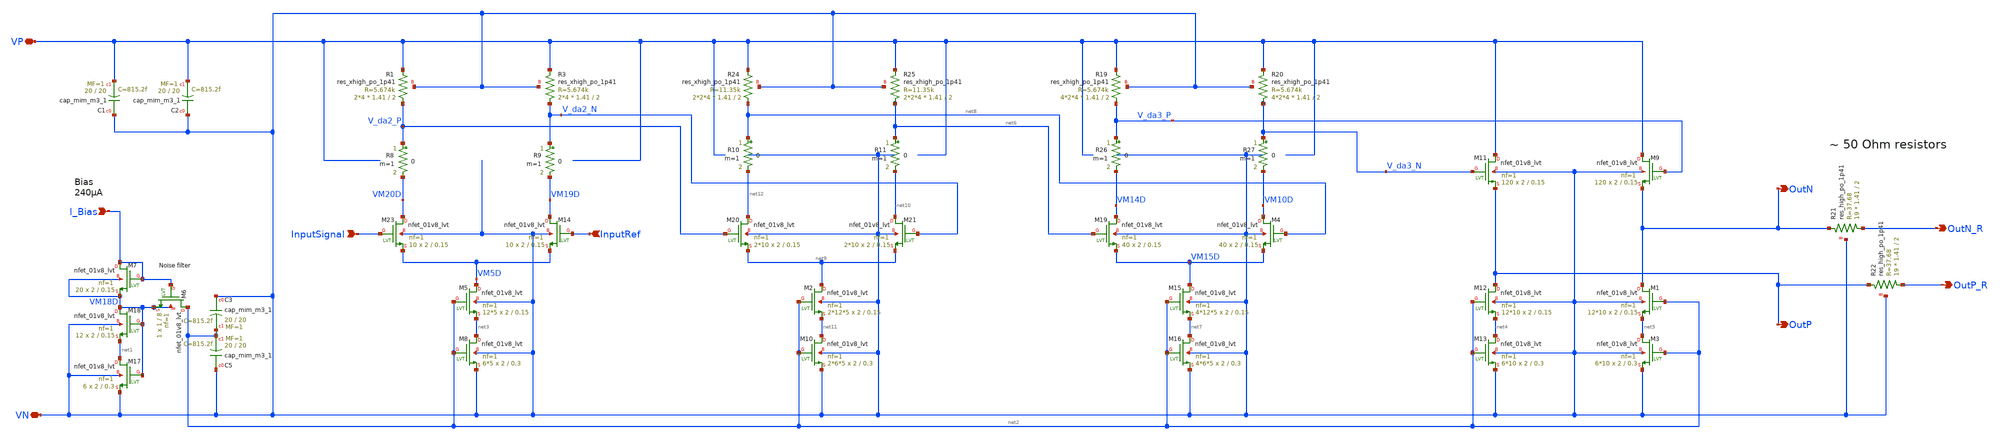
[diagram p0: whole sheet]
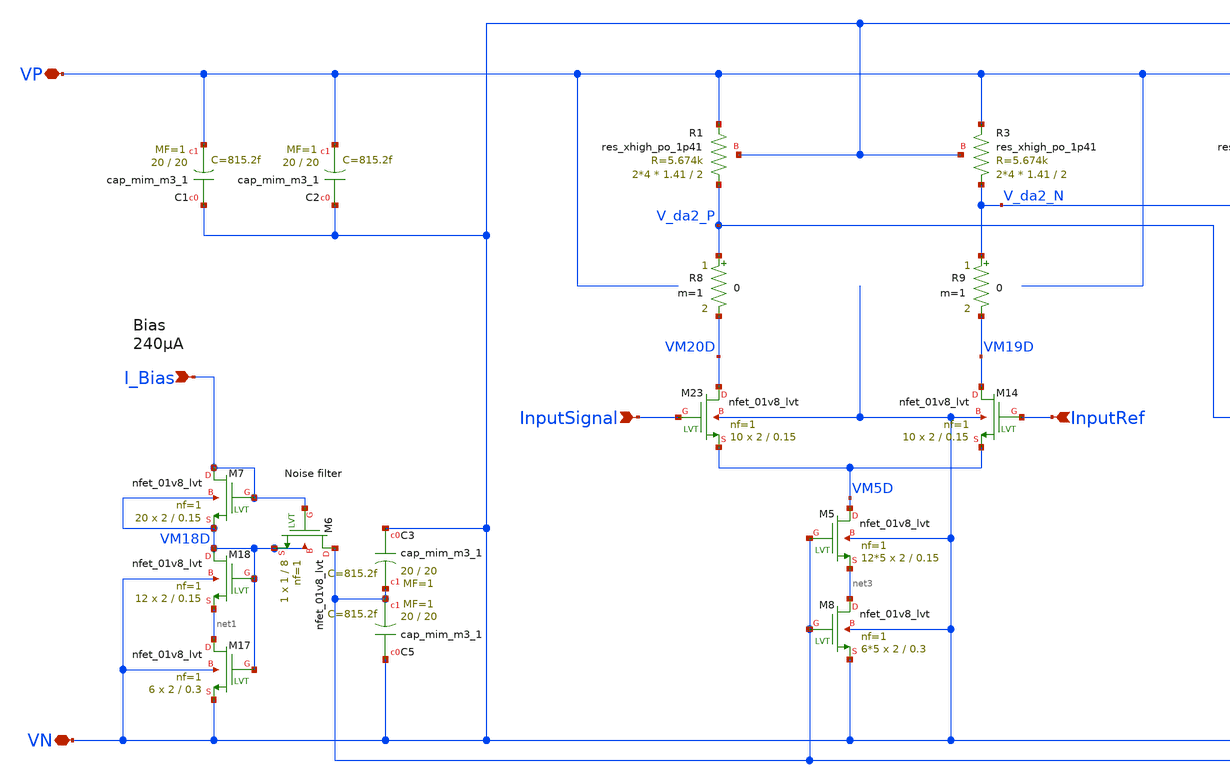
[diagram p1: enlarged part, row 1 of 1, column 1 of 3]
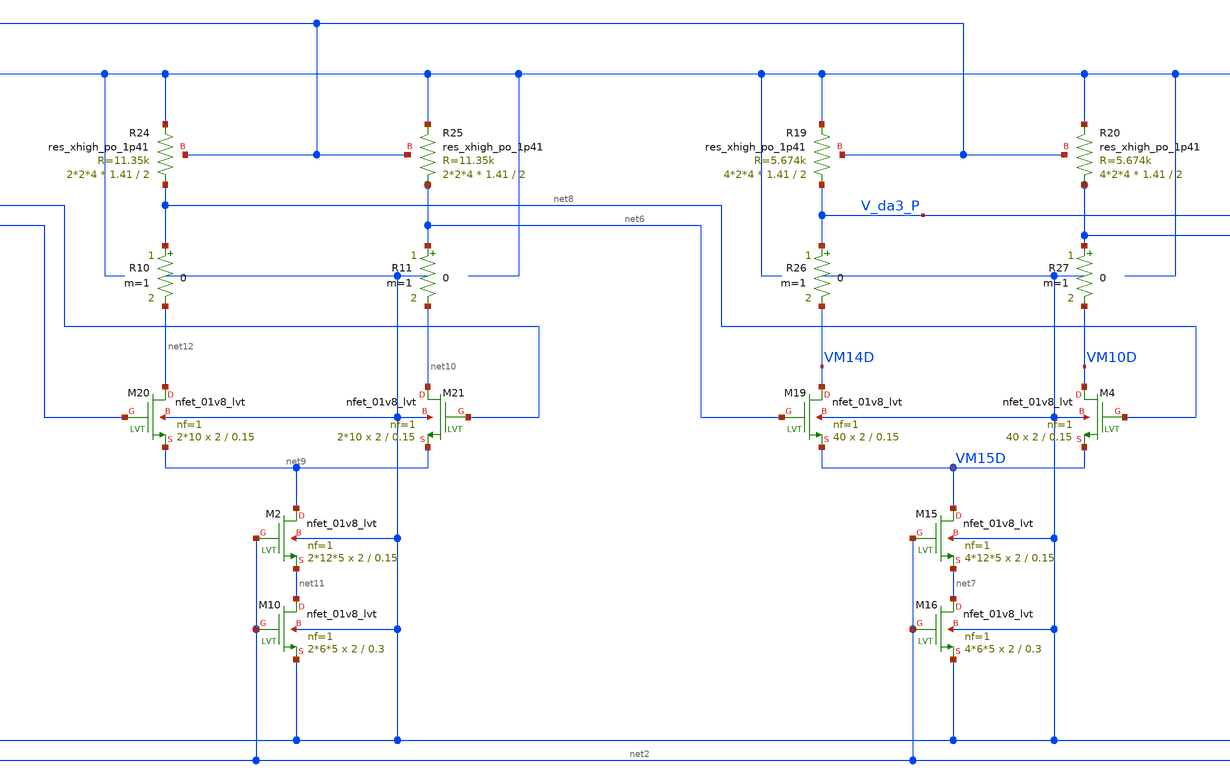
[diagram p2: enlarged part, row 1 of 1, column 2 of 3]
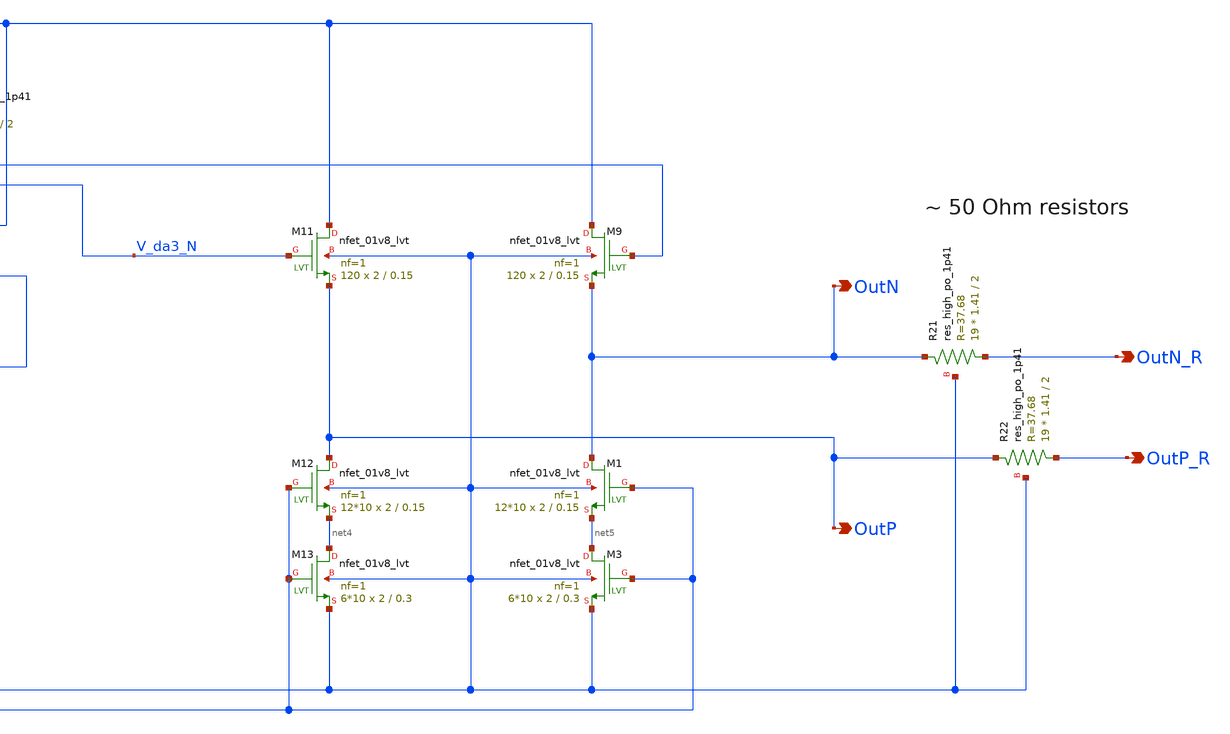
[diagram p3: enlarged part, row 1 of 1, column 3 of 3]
** sch_path: xschem/outdriver/outdriver_v4.sch
**.subckt outdriver_v4 VN InputRef VP I_Bias InputSignal OutN OutP OutN_R OutP_R
*.iopin VN
*.ipin InputRef
*.iopin VP
*.ipin I_Bias
*.ipin InputSignal
*.opin OutN
*.opin OutP
*.opin OutN_R
*.opin OutP_R
XC5 VN net2 sky130_fd_pr__cap_mim_m3_1 W=20 L=20 MF=1 m=1
XC3 VN net2 sky130_fd_pr__cap_mim_m3_1 W=20 L=20 MF=1 m=1
XM17 net1 VM18D VN VN sky130_fd_pr__nfet_01v8_lvt L=0.3 W=2 nf=1 ad='int((nf+1)/2) * W/nf * 0.29' as='int((nf+2)/2) * W/nf * 0.29'
+ pd='2*int((nf+1)/2) * (W/nf + 0.29)' ps='2*int((nf+2)/2) * (W/nf + 0.29)' nrd='0.29 / W' nrs='0.29 / W'
+ sa=0 sb=0 sd=0 mult=6 m=6
XM18 VM18D VM18D net1 VN sky130_fd_pr__nfet_01v8_lvt L=0.15 W=2 nf=1 ad='int((nf+1)/2) * W/nf * 0.29'
+ as='int((nf+2)/2) * W/nf * 0.29' pd='2*int((nf+1)/2) * (W/nf + 0.29)' ps='2*int((nf+2)/2) * (W/nf + 0.29)'
+ nrd='0.29 / W' nrs='0.29 / W' sa=0 sb=0 sd=0 mult=12 m=12
XM7 I_Bias I_Bias VM18D VM18D sky130_fd_pr__nfet_01v8_lvt L=0.15 W=2 nf=1 ad='int((nf+1)/2) * W/nf * 0.29'
+ as='int((nf+2)/2) * W/nf * 0.29' pd='2*int((nf+1)/2) * (W/nf + 0.29)' ps='2*int((nf+2)/2) * (W/nf + 0.29)'
+ nrd='0.29 / W' nrs='0.29 / W' sa=0 sb=0 sd=0 mult=20 m=20
XM5 VM5D net2 net3 VN sky130_fd_pr__nfet_01v8_lvt L=0.15 W=2 nf=1 ad='int((nf+1)/2) * W/nf * 0.29' as='int((nf+2)/2) * W/nf * 0.29'
+ pd='2*int((nf+1)/2) * (W/nf + 0.29)' ps='2*int((nf+2)/2) * (W/nf + 0.29)' nrd='0.29 / W' nrs='0.29 / W'
+ sa=0 sb=0 sd=0 mult=12*5 m=12*5
XM8 net3 net2 VN VN sky130_fd_pr__nfet_01v8_lvt L=0.3 W=2 nf=1 ad='int((nf+1)/2) * W/nf * 0.29' as='int((nf+2)/2) * W/nf * 0.29'
+ pd='2*int((nf+1)/2) * (W/nf + 0.29)' ps='2*int((nf+2)/2) * (W/nf + 0.29)' nrd='0.29 / W' nrs='0.29 / W'
+ sa=0 sb=0 sd=0 mult=6*5 m=6*5
XR1 V_da2_P VP VN sky130_fd_pr__res_xhigh_po_1p41 L=2 mult=2*4 m=2*4
XR3 V_da2_N VP VN sky130_fd_pr__res_xhigh_po_1p41 L=2 mult=2*4 m=2*4
XM9 VP V_da3_P OutN VN sky130_fd_pr__nfet_01v8_lvt L=0.15 W=2 nf=1 ad='int((nf+1)/2) * W/nf * 0.29' as='int((nf+2)/2) * W/nf * 0.29'
+ pd='2*int((nf+1)/2) * (W/nf + 0.29)' ps='2*int((nf+2)/2) * (W/nf + 0.29)' nrd='0.29 / W' nrs='0.29 / W'
+ sa=0 sb=0 sd=0 mult=120 m=120
XM11 VP V_da3_N OutP VN sky130_fd_pr__nfet_01v8_lvt L=0.15 W=2 nf=1 ad='int((nf+1)/2) * W/nf * 0.29'
+ as='int((nf+2)/2) * W/nf * 0.29' pd='2*int((nf+1)/2) * (W/nf + 0.29)' ps='2*int((nf+2)/2) * (W/nf + 0.29)'
+ nrd='0.29 / W' nrs='0.29 / W' sa=0 sb=0 sd=0 mult=120 m=120
XM12 OutP net2 net4 VN sky130_fd_pr__nfet_01v8_lvt L=0.15 W=2 nf=1 ad='int((nf+1)/2) * W/nf * 0.29' as='int((nf+2)/2) * W/nf * 0.29'
+ pd='2*int((nf+1)/2) * (W/nf + 0.29)' ps='2*int((nf+2)/2) * (W/nf + 0.29)' nrd='0.29 / W' nrs='0.29 / W'
+ sa=0 sb=0 sd=0 mult=12*10 m=12*10
XM13 net4 net2 VN VN sky130_fd_pr__nfet_01v8_lvt L=0.3 W=2 nf=1 ad='int((nf+1)/2) * W/nf * 0.29' as='int((nf+2)/2) * W/nf * 0.29'
+ pd='2*int((nf+1)/2) * (W/nf + 0.29)' ps='2*int((nf+2)/2) * (W/nf + 0.29)' nrd='0.29 / W' nrs='0.29 / W'
+ sa=0 sb=0 sd=0 mult=6*10 m=6*10
XM1 OutN net2 net5 VN sky130_fd_pr__nfet_01v8_lvt L=0.15 W=2 nf=1 ad='int((nf+1)/2) * W/nf * 0.29' as='int((nf+2)/2) * W/nf * 0.29'
+ pd='2*int((nf+1)/2) * (W/nf + 0.29)' ps='2*int((nf+2)/2) * (W/nf + 0.29)' nrd='0.29 / W' nrs='0.29 / W'
+ sa=0 sb=0 sd=0 mult=12*10 m=12*10
XM3 net5 net2 VN VN sky130_fd_pr__nfet_01v8_lvt L=0.3 W=2 nf=1 ad='int((nf+1)/2) * W/nf * 0.29' as='int((nf+2)/2) * W/nf * 0.29'
+ pd='2*int((nf+1)/2) * (W/nf + 0.29)' ps='2*int((nf+2)/2) * (W/nf + 0.29)' nrd='0.29 / W' nrs='0.29 / W'
+ sa=0 sb=0 sd=0 mult=6*10 m=6*10
XM6 net2 I_Bias VM18D VM18D sky130_fd_pr__nfet_01v8_lvt L=8 W=1 nf=1 ad='int((nf+1)/2) * W/nf * 0.29'
+ as='int((nf+2)/2) * W/nf * 0.29' pd='2*int((nf+1)/2) * (W/nf + 0.29)' ps='2*int((nf+2)/2) * (W/nf + 0.29)'
+ nrd='0.29 / W' nrs='0.29 / W' sa=0 sb=0 sd=0 mult=1 m=1
XC1 VN VP sky130_fd_pr__cap_mim_m3_1 W=20 L=20 MF=1 m=1
XC2 VN VP sky130_fd_pr__cap_mim_m3_1 W=20 L=20 MF=1 m=1
XM15 VM15D net2 net7 VN sky130_fd_pr__nfet_01v8_lvt L=0.15 W=2 nf=1 ad='int((nf+1)/2) * W/nf * 0.29'
+ as='int((nf+2)/2) * W/nf * 0.29' pd='2*int((nf+1)/2) * (W/nf + 0.29)' ps='2*int((nf+2)/2) * (W/nf + 0.29)'
+ nrd='0.29 / W' nrs='0.29 / W' sa=0 sb=0 sd=0 mult=4*12*5 m=4*12*5
XM16 net7 net2 VN VN sky130_fd_pr__nfet_01v8_lvt L=0.3 W=2 nf=1 ad='int((nf+1)/2) * W/nf * 0.29' as='int((nf+2)/2) * W/nf * 0.29'
+ pd='2*int((nf+1)/2) * (W/nf + 0.29)' ps='2*int((nf+2)/2) * (W/nf + 0.29)' nrd='0.29 / W' nrs='0.29 / W'
+ sa=0 sb=0 sd=0 mult=4*6*5 m=4*6*5
XR19 V_da3_P VP VN sky130_fd_pr__res_xhigh_po_1p41 L=2 mult=4*2*4 m=4*2*4
XR20 V_da3_N VP VN sky130_fd_pr__res_xhigh_po_1p41 L=2 mult=4*2*4 m=4*2*4
XM4 VM10D net8 VM15D VN sky130_fd_pr__nfet_01v8_lvt L=0.15 W=2 nf=1 ad='int((nf+1)/2) * W/nf * 0.29'
+ as='int((nf+2)/2) * W/nf * 0.29' pd='2*int((nf+1)/2) * (W/nf + 0.29)' ps='2*int((nf+2)/2) * (W/nf + 0.29)'
+ nrd='0.29 / W' nrs='0.29 / W' sa=0 sb=0 sd=0 mult=40 m=40
XR21 OutN_R OutN VN sky130_fd_pr__res_high_po_1p41 L=2 mult=19 m=19
XR22 OutP_R OutP VN sky130_fd_pr__res_high_po_1p41 L=2 mult=19 m=19
XM2 net9 net2 net11 VN sky130_fd_pr__nfet_01v8_lvt L=0.15 W=2 nf=1 ad='int((nf+1)/2) * W/nf * 0.29' as='int((nf+2)/2) * W/nf * 0.29'
+ pd='2*int((nf+1)/2) * (W/nf + 0.29)' ps='2*int((nf+2)/2) * (W/nf + 0.29)' nrd='0.29 / W' nrs='0.29 / W'
+ sa=0 sb=0 sd=0 mult=2*12*5 m=2*12*5
XM10 net11 net2 VN VN sky130_fd_pr__nfet_01v8_lvt L=0.3 W=2 nf=1 ad='int((nf+1)/2) * W/nf * 0.29' as='int((nf+2)/2) * W/nf * 0.29'
+ pd='2*int((nf+1)/2) * (W/nf + 0.29)' ps='2*int((nf+2)/2) * (W/nf + 0.29)' nrd='0.29 / W' nrs='0.29 / W'
+ sa=0 sb=0 sd=0 mult=2*6*5 m=2*6*5
XR24 net8 VP VN sky130_fd_pr__res_xhigh_po_1p41 L=2 mult=2*2*4 m=2*2*4
XR25 net6 VP VN sky130_fd_pr__res_xhigh_po_1p41 L=2 mult=2*2*4 m=2*2*4
XM23 VM20D InputSignal VM5D VN sky130_fd_pr__nfet_01v8_lvt L=0.15 W=2 nf=1 ad='int((nf+1)/2) * W/nf * 0.29'
+ as='int((nf+2)/2) * W/nf * 0.29' pd='2*int((nf+1)/2) * (W/nf + 0.29)' ps='2*int((nf+2)/2) * (W/nf + 0.29)'
+ nrd='0.29 / W' nrs='0.29 / W' sa=0 sb=0 sd=0 mult=10 m=10
XM19 VM14D net6 VM15D VN sky130_fd_pr__nfet_01v8_lvt L=0.15 W=2 nf=1 ad='int((nf+1)/2) * W/nf * 0.29'
+ as='int((nf+2)/2) * W/nf * 0.29' pd='2*int((nf+1)/2) * (W/nf + 0.29)' ps='2*int((nf+2)/2) * (W/nf + 0.29)'
+ nrd='0.29 / W' nrs='0.29 / W' sa=0 sb=0 sd=0 mult=40 m=40
XM14 VM19D InputRef VM5D VN sky130_fd_pr__nfet_01v8_lvt L=0.15 W=2 nf=1 ad='int((nf+1)/2) * W/nf * 0.29'
+ as='int((nf+2)/2) * W/nf * 0.29' pd='2*int((nf+1)/2) * (W/nf + 0.29)' ps='2*int((nf+2)/2) * (W/nf + 0.29)'
+ nrd='0.29 / W' nrs='0.29 / W' sa=0 sb=0 sd=0 mult=10 m=10
XM20 net12 V_da2_P net9 VN sky130_fd_pr__nfet_01v8_lvt L=0.15 W=2 nf=1 ad='int((nf+1)/2) * W/nf * 0.29'
+ as='int((nf+2)/2) * W/nf * 0.29' pd='2*int((nf+1)/2) * (W/nf + 0.29)' ps='2*int((nf+2)/2) * (W/nf + 0.29)'
+ nrd='0.29 / W' nrs='0.29 / W' sa=0 sb=0 sd=0 mult=2*10 m=2*10
XM21 net10 V_da2_N net9 VN sky130_fd_pr__nfet_01v8_lvt L=0.15 W=2 nf=1 ad='int((nf+1)/2) * W/nf * 0.29'
+ as='int((nf+2)/2) * W/nf * 0.29' pd='2*int((nf+1)/2) * (W/nf + 0.29)' ps='2*int((nf+2)/2) * (W/nf + 0.29)'
+ nrd='0.29 / W' nrs='0.29 / W' sa=0 sb=0 sd=0 mult=2*10 m=2*10
R8 V_da2_P VM20D 0 m=1
R9 V_da2_N VM19D 0 m=1
R10 net8 net12 0 m=1
R11 net6 net10 0 m=1
R26 V_da3_P VM14D 0 m=1
R27 V_da3_N VM10D 0 m=1
**.ends
.end
